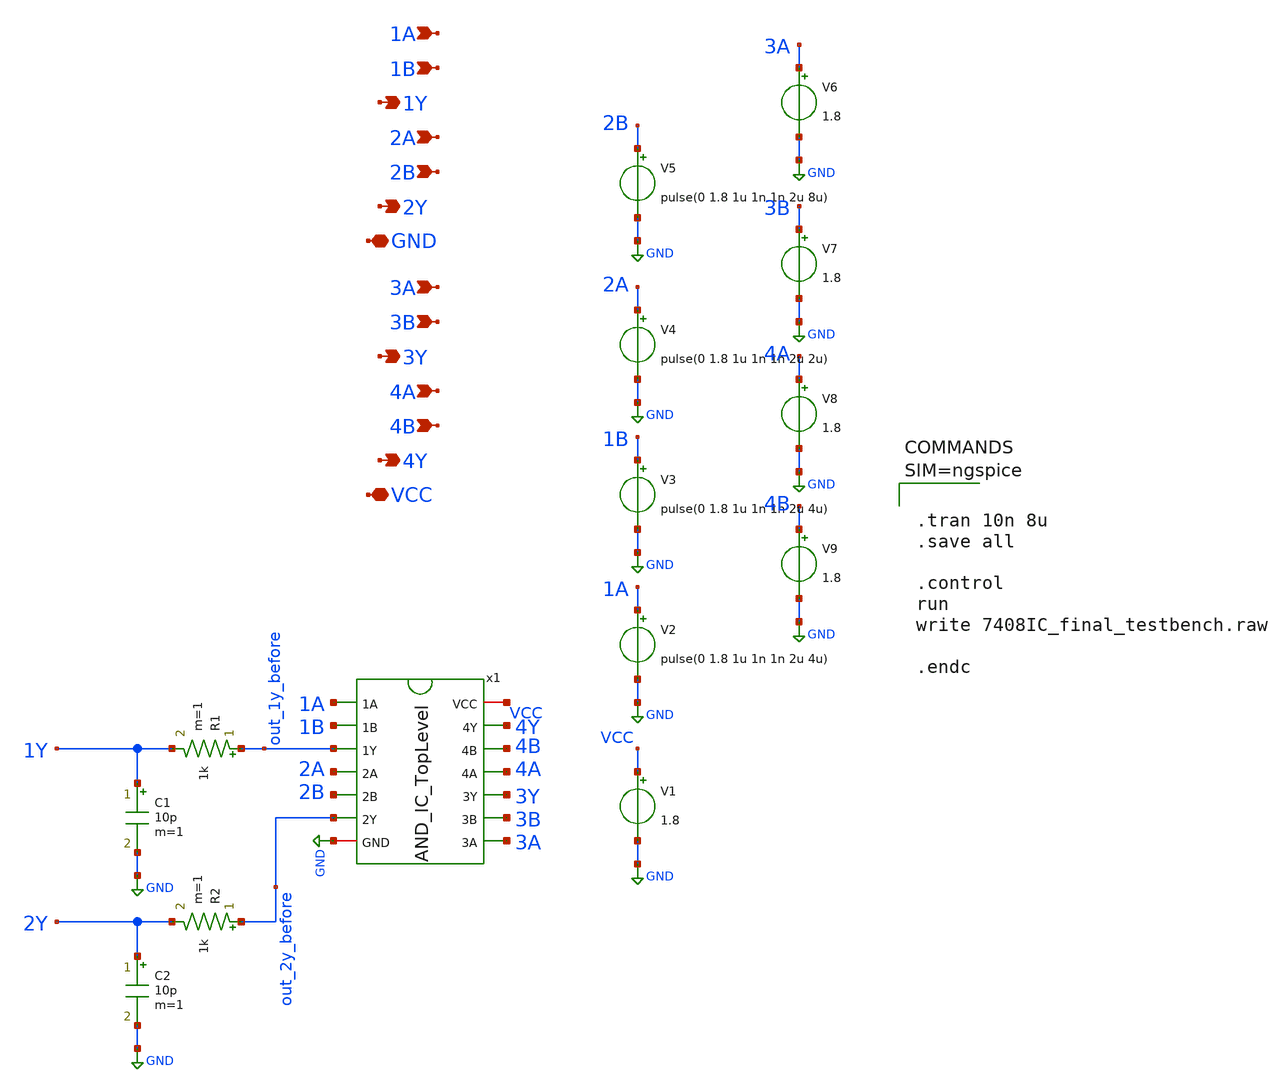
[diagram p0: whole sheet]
** sch_path: xschem/7408IC_final_testbench.sch
**.subckt 7408IC_final_testbench 1A GND 1Y 1B 2A 2B 3A 3B 4A 4B 2Y 3Y 4Y VCC
*.ipin 1A
*.iopin GND
*.opin 1Y
*.ipin 1B
*.ipin 2A
*.ipin 2B
*.ipin 3A
*.ipin 3B
*.ipin 4A
*.ipin 4B
*.opin 2Y
*.opin 3Y
*.opin 4Y
*.iopin VCC
x1 1A 1B out_1y_before 2A 2B out_2y_before GND 3A 3B 3Y 4A 4B 4Y VCC AND_IC_TopLevel
V1 VCC GND 1.8
V2 1A GND pulse(0 1.8 1u 1n 1n 2u 4u)
V3 1B GND pulse(0 1.8 1u 1n 1n 2u 4u)
V4 2A GND pulse(0 1.8 1u 1n 1n 2u 2u)
V5 2B GND pulse(0 1.8 1u 1n 1n 2u 8u)
V6 3A GND 1.8
V7 3B GND 1.8
V8 4A GND 1.8
V9 4B GND 1.8
R1 out_1y_before 1Y 1k m=1
C1 1Y GND 10p m=1
R2 out_2y_before 2Y 1k m=1
C2 2Y GND 10p m=1
**** begin user architecture code

** opencircuitdesign pdks install
.lib $::SKYWATER_MODELS/sky130.lib.spice tt





.tran 10n 8u
.save all

.control
run
write 7408IC_final_testbench.raw

.endc



**** end user architecture code
**.ends
.GLOBAL GND
.end
